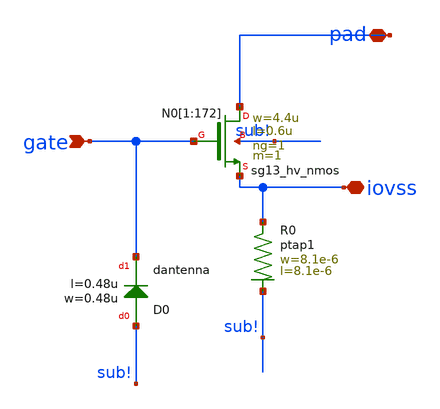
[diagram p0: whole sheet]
** sch_path: ihp-sg13g2/libs.ref/sg13g2_io/sch/xschem/sg13g2_Clamp_N43N43D4R.sch
**.subckt sg13g2_Clamp_N43N43D4R pad gate iovss
*.iopin pad
*.ipin gate
*.iopin iovss
XN0[1] pad gate iovss sub! sg13_hv_nmos w=4.4u l=0.6u ng=1 m=1 mm_ok=1
XN0[2] pad gate iovss sub! sg13_hv_nmos w=4.4u l=0.6u ng=1 m=1 mm_ok=1
XN0[3] pad gate iovss sub! sg13_hv_nmos w=4.4u l=0.6u ng=1 m=1 mm_ok=1
XN0[4] pad gate iovss sub! sg13_hv_nmos w=4.4u l=0.6u ng=1 m=1 mm_ok=1
XN0[5] pad gate iovss sub! sg13_hv_nmos w=4.4u l=0.6u ng=1 m=1 mm_ok=1
XN0[6] pad gate iovss sub! sg13_hv_nmos w=4.4u l=0.6u ng=1 m=1 mm_ok=1
XN0[7] pad gate iovss sub! sg13_hv_nmos w=4.4u l=0.6u ng=1 m=1 mm_ok=1
XN0[8] pad gate iovss sub! sg13_hv_nmos w=4.4u l=0.6u ng=1 m=1 mm_ok=1
XN0[9] pad gate iovss sub! sg13_hv_nmos w=4.4u l=0.6u ng=1 m=1 mm_ok=1
XN0[10] pad gate iovss sub! sg13_hv_nmos w=4.4u l=0.6u ng=1 m=1 mm_ok=1
XN0[11] pad gate iovss sub! sg13_hv_nmos w=4.4u l=0.6u ng=1 m=1 mm_ok=1
XN0[12] pad gate iovss sub! sg13_hv_nmos w=4.4u l=0.6u ng=1 m=1 mm_ok=1
XN0[13] pad gate iovss sub! sg13_hv_nmos w=4.4u l=0.6u ng=1 m=1 mm_ok=1
XN0[14] pad gate iovss sub! sg13_hv_nmos w=4.4u l=0.6u ng=1 m=1 mm_ok=1
XN0[15] pad gate iovss sub! sg13_hv_nmos w=4.4u l=0.6u ng=1 m=1 mm_ok=1
XN0[16] pad gate iovss sub! sg13_hv_nmos w=4.4u l=0.6u ng=1 m=1 mm_ok=1
XN0[17] pad gate iovss sub! sg13_hv_nmos w=4.4u l=0.6u ng=1 m=1 mm_ok=1
XN0[18] pad gate iovss sub! sg13_hv_nmos w=4.4u l=0.6u ng=1 m=1 mm_ok=1
XN0[19] pad gate iovss sub! sg13_hv_nmos w=4.4u l=0.6u ng=1 m=1 mm_ok=1
XN0[20] pad gate iovss sub! sg13_hv_nmos w=4.4u l=0.6u ng=1 m=1 mm_ok=1
XN0[21] pad gate iovss sub! sg13_hv_nmos w=4.4u l=0.6u ng=1 m=1 mm_ok=1
XN0[22] pad gate iovss sub! sg13_hv_nmos w=4.4u l=0.6u ng=1 m=1 mm_ok=1
XN0[23] pad gate iovss sub! sg13_hv_nmos w=4.4u l=0.6u ng=1 m=1 mm_ok=1
XN0[24] pad gate iovss sub! sg13_hv_nmos w=4.4u l=0.6u ng=1 m=1 mm_ok=1
XN0[25] pad gate iovss sub! sg13_hv_nmos w=4.4u l=0.6u ng=1 m=1 mm_ok=1
XN0[26] pad gate iovss sub! sg13_hv_nmos w=4.4u l=0.6u ng=1 m=1 mm_ok=1
XN0[27] pad gate iovss sub! sg13_hv_nmos w=4.4u l=0.6u ng=1 m=1 mm_ok=1
XN0[28] pad gate iovss sub! sg13_hv_nmos w=4.4u l=0.6u ng=1 m=1 mm_ok=1
XN0[29] pad gate iovss sub! sg13_hv_nmos w=4.4u l=0.6u ng=1 m=1 mm_ok=1
XN0[30] pad gate iovss sub! sg13_hv_nmos w=4.4u l=0.6u ng=1 m=1 mm_ok=1
XN0[31] pad gate iovss sub! sg13_hv_nmos w=4.4u l=0.6u ng=1 m=1 mm_ok=1
XN0[32] pad gate iovss sub! sg13_hv_nmos w=4.4u l=0.6u ng=1 m=1 mm_ok=1
XN0[33] pad gate iovss sub! sg13_hv_nmos w=4.4u l=0.6u ng=1 m=1 mm_ok=1
XN0[34] pad gate iovss sub! sg13_hv_nmos w=4.4u l=0.6u ng=1 m=1 mm_ok=1
XN0[35] pad gate iovss sub! sg13_hv_nmos w=4.4u l=0.6u ng=1 m=1 mm_ok=1
XN0[36] pad gate iovss sub! sg13_hv_nmos w=4.4u l=0.6u ng=1 m=1 mm_ok=1
XN0[37] pad gate iovss sub! sg13_hv_nmos w=4.4u l=0.6u ng=1 m=1 mm_ok=1
XN0[38] pad gate iovss sub! sg13_hv_nmos w=4.4u l=0.6u ng=1 m=1 mm_ok=1
XN0[39] pad gate iovss sub! sg13_hv_nmos w=4.4u l=0.6u ng=1 m=1 mm_ok=1
XN0[40] pad gate iovss sub! sg13_hv_nmos w=4.4u l=0.6u ng=1 m=1 mm_ok=1
XN0[41] pad gate iovss sub! sg13_hv_nmos w=4.4u l=0.6u ng=1 m=1 mm_ok=1
XN0[42] pad gate iovss sub! sg13_hv_nmos w=4.4u l=0.6u ng=1 m=1 mm_ok=1
XN0[43] pad gate iovss sub! sg13_hv_nmos w=4.4u l=0.6u ng=1 m=1 mm_ok=1
XN0[44] pad gate iovss sub! sg13_hv_nmos w=4.4u l=0.6u ng=1 m=1 mm_ok=1
XN0[45] pad gate iovss sub! sg13_hv_nmos w=4.4u l=0.6u ng=1 m=1 mm_ok=1
XN0[46] pad gate iovss sub! sg13_hv_nmos w=4.4u l=0.6u ng=1 m=1 mm_ok=1
XN0[47] pad gate iovss sub! sg13_hv_nmos w=4.4u l=0.6u ng=1 m=1 mm_ok=1
XN0[48] pad gate iovss sub! sg13_hv_nmos w=4.4u l=0.6u ng=1 m=1 mm_ok=1
XN0[49] pad gate iovss sub! sg13_hv_nmos w=4.4u l=0.6u ng=1 m=1 mm_ok=1
XN0[50] pad gate iovss sub! sg13_hv_nmos w=4.4u l=0.6u ng=1 m=1 mm_ok=1
XN0[51] pad gate iovss sub! sg13_hv_nmos w=4.4u l=0.6u ng=1 m=1 mm_ok=1
XN0[52] pad gate iovss sub! sg13_hv_nmos w=4.4u l=0.6u ng=1 m=1 mm_ok=1
XN0[53] pad gate iovss sub! sg13_hv_nmos w=4.4u l=0.6u ng=1 m=1 mm_ok=1
XN0[54] pad gate iovss sub! sg13_hv_nmos w=4.4u l=0.6u ng=1 m=1 mm_ok=1
XN0[55] pad gate iovss sub! sg13_hv_nmos w=4.4u l=0.6u ng=1 m=1 mm_ok=1
XN0[56] pad gate iovss sub! sg13_hv_nmos w=4.4u l=0.6u ng=1 m=1 mm_ok=1
XN0[57] pad gate iovss sub! sg13_hv_nmos w=4.4u l=0.6u ng=1 m=1 mm_ok=1
XN0[58] pad gate iovss sub! sg13_hv_nmos w=4.4u l=0.6u ng=1 m=1 mm_ok=1
XN0[59] pad gate iovss sub! sg13_hv_nmos w=4.4u l=0.6u ng=1 m=1 mm_ok=1
XN0[60] pad gate iovss sub! sg13_hv_nmos w=4.4u l=0.6u ng=1 m=1 mm_ok=1
XN0[61] pad gate iovss sub! sg13_hv_nmos w=4.4u l=0.6u ng=1 m=1 mm_ok=1
XN0[62] pad gate iovss sub! sg13_hv_nmos w=4.4u l=0.6u ng=1 m=1 mm_ok=1
XN0[63] pad gate iovss sub! sg13_hv_nmos w=4.4u l=0.6u ng=1 m=1 mm_ok=1
XN0[64] pad gate iovss sub! sg13_hv_nmos w=4.4u l=0.6u ng=1 m=1 mm_ok=1
XN0[65] pad gate iovss sub! sg13_hv_nmos w=4.4u l=0.6u ng=1 m=1 mm_ok=1
XN0[66] pad gate iovss sub! sg13_hv_nmos w=4.4u l=0.6u ng=1 m=1 mm_ok=1
XN0[67] pad gate iovss sub! sg13_hv_nmos w=4.4u l=0.6u ng=1 m=1 mm_ok=1
XN0[68] pad gate iovss sub! sg13_hv_nmos w=4.4u l=0.6u ng=1 m=1 mm_ok=1
XN0[69] pad gate iovss sub! sg13_hv_nmos w=4.4u l=0.6u ng=1 m=1 mm_ok=1
XN0[70] pad gate iovss sub! sg13_hv_nmos w=4.4u l=0.6u ng=1 m=1 mm_ok=1
XN0[71] pad gate iovss sub! sg13_hv_nmos w=4.4u l=0.6u ng=1 m=1 mm_ok=1
XN0[72] pad gate iovss sub! sg13_hv_nmos w=4.4u l=0.6u ng=1 m=1 mm_ok=1
XN0[73] pad gate iovss sub! sg13_hv_nmos w=4.4u l=0.6u ng=1 m=1 mm_ok=1
XN0[74] pad gate iovss sub! sg13_hv_nmos w=4.4u l=0.6u ng=1 m=1 mm_ok=1
XN0[75] pad gate iovss sub! sg13_hv_nmos w=4.4u l=0.6u ng=1 m=1 mm_ok=1
XN0[76] pad gate iovss sub! sg13_hv_nmos w=4.4u l=0.6u ng=1 m=1 mm_ok=1
XN0[77] pad gate iovss sub! sg13_hv_nmos w=4.4u l=0.6u ng=1 m=1 mm_ok=1
XN0[78] pad gate iovss sub! sg13_hv_nmos w=4.4u l=0.6u ng=1 m=1 mm_ok=1
XN0[79] pad gate iovss sub! sg13_hv_nmos w=4.4u l=0.6u ng=1 m=1 mm_ok=1
XN0[80] pad gate iovss sub! sg13_hv_nmos w=4.4u l=0.6u ng=1 m=1 mm_ok=1
XN0[81] pad gate iovss sub! sg13_hv_nmos w=4.4u l=0.6u ng=1 m=1 mm_ok=1
XN0[82] pad gate iovss sub! sg13_hv_nmos w=4.4u l=0.6u ng=1 m=1 mm_ok=1
XN0[83] pad gate iovss sub! sg13_hv_nmos w=4.4u l=0.6u ng=1 m=1 mm_ok=1
XN0[84] pad gate iovss sub! sg13_hv_nmos w=4.4u l=0.6u ng=1 m=1 mm_ok=1
XN0[85] pad gate iovss sub! sg13_hv_nmos w=4.4u l=0.6u ng=1 m=1 mm_ok=1
XN0[86] pad gate iovss sub! sg13_hv_nmos w=4.4u l=0.6u ng=1 m=1 mm_ok=1
XN0[87] pad gate iovss sub! sg13_hv_nmos w=4.4u l=0.6u ng=1 m=1 mm_ok=1
XN0[88] pad gate iovss sub! sg13_hv_nmos w=4.4u l=0.6u ng=1 m=1 mm_ok=1
XN0[89] pad gate iovss sub! sg13_hv_nmos w=4.4u l=0.6u ng=1 m=1 mm_ok=1
XN0[90] pad gate iovss sub! sg13_hv_nmos w=4.4u l=0.6u ng=1 m=1 mm_ok=1
XN0[91] pad gate iovss sub! sg13_hv_nmos w=4.4u l=0.6u ng=1 m=1 mm_ok=1
XN0[92] pad gate iovss sub! sg13_hv_nmos w=4.4u l=0.6u ng=1 m=1 mm_ok=1
XN0[93] pad gate iovss sub! sg13_hv_nmos w=4.4u l=0.6u ng=1 m=1 mm_ok=1
XN0[94] pad gate iovss sub! sg13_hv_nmos w=4.4u l=0.6u ng=1 m=1 mm_ok=1
XN0[95] pad gate iovss sub! sg13_hv_nmos w=4.4u l=0.6u ng=1 m=1 mm_ok=1
XN0[96] pad gate iovss sub! sg13_hv_nmos w=4.4u l=0.6u ng=1 m=1 mm_ok=1
XN0[97] pad gate iovss sub! sg13_hv_nmos w=4.4u l=0.6u ng=1 m=1 mm_ok=1
XN0[98] pad gate iovss sub! sg13_hv_nmos w=4.4u l=0.6u ng=1 m=1 mm_ok=1
XN0[99] pad gate iovss sub! sg13_hv_nmos w=4.4u l=0.6u ng=1 m=1 mm_ok=1
XN0[100] pad gate iovss sub! sg13_hv_nmos w=4.4u l=0.6u ng=1 m=1 mm_ok=1
XN0[101] pad gate iovss sub! sg13_hv_nmos w=4.4u l=0.6u ng=1 m=1 mm_ok=1
XN0[102] pad gate iovss sub! sg13_hv_nmos w=4.4u l=0.6u ng=1 m=1 mm_ok=1
XN0[103] pad gate iovss sub! sg13_hv_nmos w=4.4u l=0.6u ng=1 m=1 mm_ok=1
XN0[104] pad gate iovss sub! sg13_hv_nmos w=4.4u l=0.6u ng=1 m=1 mm_ok=1
XN0[105] pad gate iovss sub! sg13_hv_nmos w=4.4u l=0.6u ng=1 m=1 mm_ok=1
XN0[106] pad gate iovss sub! sg13_hv_nmos w=4.4u l=0.6u ng=1 m=1 mm_ok=1
XN0[107] pad gate iovss sub! sg13_hv_nmos w=4.4u l=0.6u ng=1 m=1 mm_ok=1
XN0[108] pad gate iovss sub! sg13_hv_nmos w=4.4u l=0.6u ng=1 m=1 mm_ok=1
XN0[109] pad gate iovss sub! sg13_hv_nmos w=4.4u l=0.6u ng=1 m=1 mm_ok=1
XN0[110] pad gate iovss sub! sg13_hv_nmos w=4.4u l=0.6u ng=1 m=1 mm_ok=1
XN0[111] pad gate iovss sub! sg13_hv_nmos w=4.4u l=0.6u ng=1 m=1 mm_ok=1
XN0[112] pad gate iovss sub! sg13_hv_nmos w=4.4u l=0.6u ng=1 m=1 mm_ok=1
XN0[113] pad gate iovss sub! sg13_hv_nmos w=4.4u l=0.6u ng=1 m=1 mm_ok=1
XN0[114] pad gate iovss sub! sg13_hv_nmos w=4.4u l=0.6u ng=1 m=1 mm_ok=1
XN0[115] pad gate iovss sub! sg13_hv_nmos w=4.4u l=0.6u ng=1 m=1 mm_ok=1
XN0[116] pad gate iovss sub! sg13_hv_nmos w=4.4u l=0.6u ng=1 m=1 mm_ok=1
XN0[117] pad gate iovss sub! sg13_hv_nmos w=4.4u l=0.6u ng=1 m=1 mm_ok=1
XN0[118] pad gate iovss sub! sg13_hv_nmos w=4.4u l=0.6u ng=1 m=1 mm_ok=1
XN0[119] pad gate iovss sub! sg13_hv_nmos w=4.4u l=0.6u ng=1 m=1 mm_ok=1
XN0[120] pad gate iovss sub! sg13_hv_nmos w=4.4u l=0.6u ng=1 m=1 mm_ok=1
XN0[121] pad gate iovss sub! sg13_hv_nmos w=4.4u l=0.6u ng=1 m=1 mm_ok=1
XN0[122] pad gate iovss sub! sg13_hv_nmos w=4.4u l=0.6u ng=1 m=1 mm_ok=1
XN0[123] pad gate iovss sub! sg13_hv_nmos w=4.4u l=0.6u ng=1 m=1 mm_ok=1
XN0[124] pad gate iovss sub! sg13_hv_nmos w=4.4u l=0.6u ng=1 m=1 mm_ok=1
XN0[125] pad gate iovss sub! sg13_hv_nmos w=4.4u l=0.6u ng=1 m=1 mm_ok=1
XN0[126] pad gate iovss sub! sg13_hv_nmos w=4.4u l=0.6u ng=1 m=1 mm_ok=1
XN0[127] pad gate iovss sub! sg13_hv_nmos w=4.4u l=0.6u ng=1 m=1 mm_ok=1
XN0[128] pad gate iovss sub! sg13_hv_nmos w=4.4u l=0.6u ng=1 m=1 mm_ok=1
XN0[129] pad gate iovss sub! sg13_hv_nmos w=4.4u l=0.6u ng=1 m=1 mm_ok=1
XN0[130] pad gate iovss sub! sg13_hv_nmos w=4.4u l=0.6u ng=1 m=1 mm_ok=1
XN0[131] pad gate iovss sub! sg13_hv_nmos w=4.4u l=0.6u ng=1 m=1 mm_ok=1
XN0[132] pad gate iovss sub! sg13_hv_nmos w=4.4u l=0.6u ng=1 m=1 mm_ok=1
XN0[133] pad gate iovss sub! sg13_hv_nmos w=4.4u l=0.6u ng=1 m=1 mm_ok=1
XN0[134] pad gate iovss sub! sg13_hv_nmos w=4.4u l=0.6u ng=1 m=1 mm_ok=1
XN0[135] pad gate iovss sub! sg13_hv_nmos w=4.4u l=0.6u ng=1 m=1 mm_ok=1
XN0[136] pad gate iovss sub! sg13_hv_nmos w=4.4u l=0.6u ng=1 m=1 mm_ok=1
XN0[137] pad gate iovss sub! sg13_hv_nmos w=4.4u l=0.6u ng=1 m=1 mm_ok=1
XN0[138] pad gate iovss sub! sg13_hv_nmos w=4.4u l=0.6u ng=1 m=1 mm_ok=1
XN0[139] pad gate iovss sub! sg13_hv_nmos w=4.4u l=0.6u ng=1 m=1 mm_ok=1
XN0[140] pad gate iovss sub! sg13_hv_nmos w=4.4u l=0.6u ng=1 m=1 mm_ok=1
XN0[141] pad gate iovss sub! sg13_hv_nmos w=4.4u l=0.6u ng=1 m=1 mm_ok=1
XN0[142] pad gate iovss sub! sg13_hv_nmos w=4.4u l=0.6u ng=1 m=1 mm_ok=1
XN0[143] pad gate iovss sub! sg13_hv_nmos w=4.4u l=0.6u ng=1 m=1 mm_ok=1
XN0[144] pad gate iovss sub! sg13_hv_nmos w=4.4u l=0.6u ng=1 m=1 mm_ok=1
XN0[145] pad gate iovss sub! sg13_hv_nmos w=4.4u l=0.6u ng=1 m=1 mm_ok=1
XN0[146] pad gate iovss sub! sg13_hv_nmos w=4.4u l=0.6u ng=1 m=1 mm_ok=1
XN0[147] pad gate iovss sub! sg13_hv_nmos w=4.4u l=0.6u ng=1 m=1 mm_ok=1
XN0[148] pad gate iovss sub! sg13_hv_nmos w=4.4u l=0.6u ng=1 m=1 mm_ok=1
XN0[149] pad gate iovss sub! sg13_hv_nmos w=4.4u l=0.6u ng=1 m=1 mm_ok=1
XN0[150] pad gate iovss sub! sg13_hv_nmos w=4.4u l=0.6u ng=1 m=1 mm_ok=1
XN0[151] pad gate iovss sub! sg13_hv_nmos w=4.4u l=0.6u ng=1 m=1 mm_ok=1
XN0[152] pad gate iovss sub! sg13_hv_nmos w=4.4u l=0.6u ng=1 m=1 mm_ok=1
XN0[153] pad gate iovss sub! sg13_hv_nmos w=4.4u l=0.6u ng=1 m=1 mm_ok=1
XN0[154] pad gate iovss sub! sg13_hv_nmos w=4.4u l=0.6u ng=1 m=1 mm_ok=1
XN0[155] pad gate iovss sub! sg13_hv_nmos w=4.4u l=0.6u ng=1 m=1 mm_ok=1
XN0[156] pad gate iovss sub! sg13_hv_nmos w=4.4u l=0.6u ng=1 m=1 mm_ok=1
XN0[157] pad gate iovss sub! sg13_hv_nmos w=4.4u l=0.6u ng=1 m=1 mm_ok=1
XN0[158] pad gate iovss sub! sg13_hv_nmos w=4.4u l=0.6u ng=1 m=1 mm_ok=1
XN0[159] pad gate iovss sub! sg13_hv_nmos w=4.4u l=0.6u ng=1 m=1 mm_ok=1
XN0[160] pad gate iovss sub! sg13_hv_nmos w=4.4u l=0.6u ng=1 m=1 mm_ok=1
XN0[161] pad gate iovss sub! sg13_hv_nmos w=4.4u l=0.6u ng=1 m=1 mm_ok=1
XN0[162] pad gate iovss sub! sg13_hv_nmos w=4.4u l=0.6u ng=1 m=1 mm_ok=1
XN0[163] pad gate iovss sub! sg13_hv_nmos w=4.4u l=0.6u ng=1 m=1 mm_ok=1
XN0[164] pad gate iovss sub! sg13_hv_nmos w=4.4u l=0.6u ng=1 m=1 mm_ok=1
XN0[165] pad gate iovss sub! sg13_hv_nmos w=4.4u l=0.6u ng=1 m=1 mm_ok=1
XN0[166] pad gate iovss sub! sg13_hv_nmos w=4.4u l=0.6u ng=1 m=1 mm_ok=1
XN0[167] pad gate iovss sub! sg13_hv_nmos w=4.4u l=0.6u ng=1 m=1 mm_ok=1
XN0[168] pad gate iovss sub! sg13_hv_nmos w=4.4u l=0.6u ng=1 m=1 mm_ok=1
XN0[169] pad gate iovss sub! sg13_hv_nmos w=4.4u l=0.6u ng=1 m=1 mm_ok=1
XN0[170] pad gate iovss sub! sg13_hv_nmos w=4.4u l=0.6u ng=1 m=1 mm_ok=1
XN0[171] pad gate iovss sub! sg13_hv_nmos w=4.4u l=0.6u ng=1 m=1 mm_ok=1
XN0[172] pad gate iovss sub! sg13_hv_nmos w=4.4u l=0.6u ng=1 m=1 mm_ok=1
XD0 sub! gate dantenna l=0.48u w=0.48u
XR0 iovss sub! ptap1 R=9.999 w=8.1e-6 l=8.1e-6
**.ends
.end
